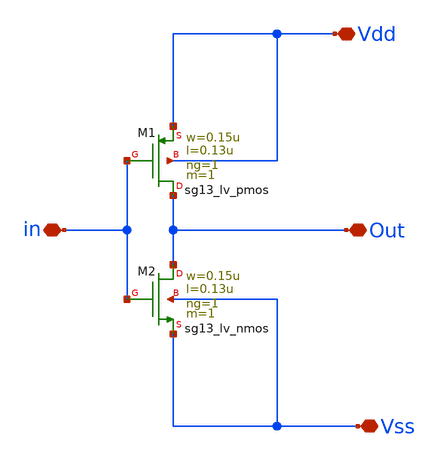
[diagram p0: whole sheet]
** sch_path: design/blocks/inversor/untitled.sch
**.subckt untitled Vdd Out Vss in
*.iopin Vdd
*.iopin Out
*.iopin Vss
*.iopin in
XM1 Out in Vdd Vdd sg13_lv_pmos w=0.15u l=0.13u ng=1 m=1 mm_ok=1
XM2 Out in Vss Vss sg13_lv_nmos w=0.15u l=0.13u ng=1 m=1 mm_ok=1
**.ends
.end
